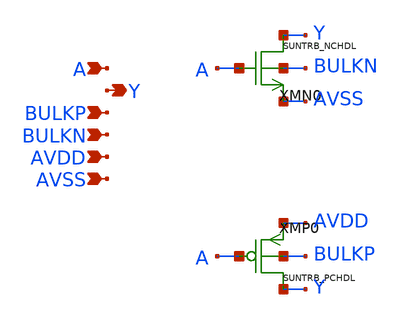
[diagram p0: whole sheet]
** sch_path: design/SUN_TRB_SKY130NM/SUNTRB_IVX1_CV.sch
**.subckt SUNTRB_IVX1_CV A Y BULKP BULKN AVDD AVSS
*.ipin A
*.opin Y
*.ipin BULKP
*.ipin BULKN
*.ipin AVDD
*.ipin AVSS
XMN0 Y A AVSS BULKN SUNTRB_NCHDL xoffset=0 yoffset=0 angle=0
XMP0 Y A AVDD BULKP SUNTRB_PCHDL xoffset=0 yoffset=0 angle=0 M=1
**.ends
.end
